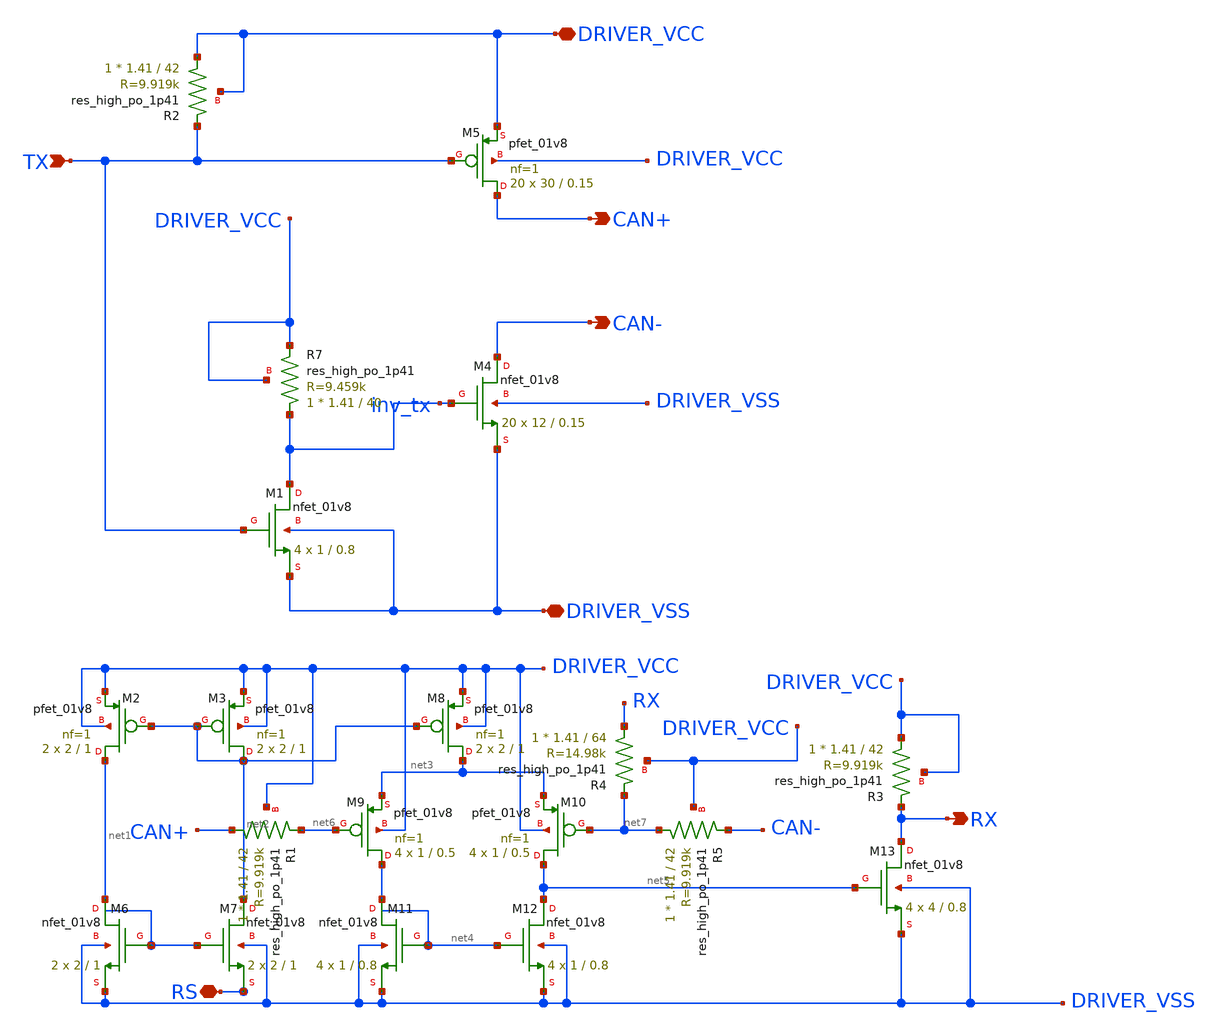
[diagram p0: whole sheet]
** sch_path: ISSCC26/submitted_notebooks/Opensource-ULP-CAN_Transceiver/xschem/can_ic/can_ic.sch
**.subckt can_ic DRIVER_VCC DRIVER_VSS TX CAN+ CAN- RS RX
*.iopin DRIVER_VCC
*.iopin DRIVER_VSS
*.ipin TX
*.opin CAN+
*.opin CAN-
*.iopin RS
*.opin RX
XM4 CAN- inv_tx DRIVER_VSS DRIVER_VSS sky130_fd_pr__nfet_01v8 W=12 L=0.15 ad='int((1 + 1)/2) * 12 / 1 * 0.29'
+ pd='2*int((1 + 1)/2) * (12 / 1 + 0.29)' as='int((1 + 2)/2) * 12 / 1 * 0.29' ps='2*int((1 + 2)/2) * (12 / 1 + 0.29)'
+ nrd='0.29 / 12 ' nrs='0.29 / 12 ' sa=0 sb=0 sd=0 nf=1 mult=20
XM5 CAN+ TX DRIVER_VCC DRIVER_VCC sky130_fd_pr__pfet_01v8 L=0.15 W=30 nf=1 ad='int((1 + 1)/2) * 30 / 1 * 0.29'
+ as='int((1 + 2)/2) * 30 / 1 * 0.29' pd='2*int((1 + 1)/2) * (30 / 1 + 0.29)' ps='2*int((1 + 2)/2) * (30 / 1 + 0.29)'
+ nrd='0.29 / 30 ' nrs='0.29 / 30 ' sa=0 sb=0 sd=0 mult=20 m=20
XM1 inv_tx TX DRIVER_VSS DRIVER_VSS sky130_fd_pr__nfet_01v8 W=1 L=0.8 ad='int((1 + 1)/2) * 1 / 1 * 0.29'
+ pd='2*int((1 + 1)/2) * (1 / 1 + 0.29)' as='int((1 + 2)/2) * 1 / 1 * 0.29' ps='2*int((1 + 2)/2) * (1 / 1 + 0.29)'
+ nrd='0.29 / 1 ' nrs='0.29 / 1 ' sa=0 sb=0 sd=0 nf=1 mult=4
XM2 net1 net2 DRIVER_VCC DRIVER_VCC sky130_fd_pr__pfet_01v8 L=1 W=2 nf=1 ad='int((nf+1)/2) * W/nf * 0.29'
+ as='int((nf+2)/2) * W/nf * 0.29' pd='2*int((nf+1)/2) * (W/nf + 0.29)' ps='2*int((nf+2)/2) * (W/nf + 0.29)'
+ nrd='0.29 / W' nrs='0.29 / W' sa=0 sb=0 sd=0 mult=2 m=2
XM3 net2 net2 DRIVER_VCC DRIVER_VCC sky130_fd_pr__pfet_01v8 L=1 W=2 nf=1 ad='int((nf+1)/2) * W/nf * 0.29'
+ as='int((nf+2)/2) * W/nf * 0.29' pd='2*int((nf+1)/2) * (W/nf + 0.29)' ps='2*int((nf+2)/2) * (W/nf + 0.29)'
+ nrd='0.29 / W' nrs='0.29 / W' sa=0 sb=0 sd=0 mult=2 m=2
XM6 net1 net1 DRIVER_VSS DRIVER_VSS sky130_fd_pr__nfet_01v8 W=2 L=1 ad='int((nf+1)/2) * W/nf * 0.29'
+ pd='2*int((nf+1)/2) * (W/nf + 0.29)' as='int((nf+2)/2) * W/nf * 0.29' ps='2*int((nf+2)/2) * (W/nf + 0.29)'
+ nrd='0.29 / W' nrs='0.29 / W' sa=0 sb=0 sd=0 nf=1 mult=2
XM7 net2 net1 RS DRIVER_VSS sky130_fd_pr__nfet_01v8 W=2 L=1 ad='int((nf+1)/2) * W/nf * 0.29' pd='2*int((nf+1)/2) * (W/nf + 0.29)'
+ as='int((nf+2)/2) * W/nf * 0.29' ps='2*int((nf+2)/2) * (W/nf + 0.29)' nrd='0.29 / W' nrs='0.29 / W' sa=0
+ sb=0 sd=0 nf=1 mult=2
XM8 net3 net2 DRIVER_VCC DRIVER_VCC sky130_fd_pr__pfet_01v8 L=1 W=2 nf=1 ad='int((nf+1)/2) * W/nf * 0.29'
+ as='int((nf+2)/2) * W/nf * 0.29' pd='2*int((nf+1)/2) * (W/nf + 0.29)' ps='2*int((nf+2)/2) * (W/nf + 0.29)'
+ nrd='0.29 / W' nrs='0.29 / W' sa=0 sb=0 sd=0 mult=2 m=2
XM9 net4 net6 net3 DRIVER_VCC sky130_fd_pr__pfet_01v8 L=0.5 W=1 nf=1 ad='int((nf+1)/2) * W/nf * 0.29'
+ as='int((nf+2)/2) * W/nf * 0.29' pd='2*int((nf+1)/2) * (W/nf + 0.29)' ps='2*int((nf+2)/2) * (W/nf + 0.29)'
+ nrd='0.29 / W' nrs='0.29 / W' sa=0 sb=0 sd=0 mult=4 m=4
XM10 net5 net7 net3 DRIVER_VCC sky130_fd_pr__pfet_01v8 L=0.5 W=1 nf=1 ad='int((nf+1)/2) * W/nf * 0.29'
+ as='int((nf+2)/2) * W/nf * 0.29' pd='2*int((nf+1)/2) * (W/nf + 0.29)' ps='2*int((nf+2)/2) * (W/nf + 0.29)'
+ nrd='0.29 / W' nrs='0.29 / W' sa=0 sb=0 sd=0 mult=4 m=4
XM11 net4 net4 DRIVER_VSS DRIVER_VSS sky130_fd_pr__nfet_01v8 W=1 L=0.8 ad='int((nf+1)/2) * W/nf * 0.29'
+ pd='2*int((nf+1)/2) * (W/nf + 0.29)' as='int((nf+2)/2) * W/nf * 0.29' ps='2*int((nf+2)/2) * (W/nf + 0.29)'
+ nrd='0.29 / W' nrs='0.29 / W' sa=0 sb=0 sd=0 nf=1 mult=4
XM12 net5 net4 DRIVER_VSS DRIVER_VSS sky130_fd_pr__nfet_01v8 W=1 L=0.8 ad='int((nf+1)/2) * W/nf * 0.29'
+ pd='2*int((nf+1)/2) * (W/nf + 0.29)' as='int((nf+2)/2) * W/nf * 0.29' ps='2*int((nf+2)/2) * (W/nf + 0.29)'
+ nrd='0.29 / W' nrs='0.29 / W' sa=0 sb=0 sd=0 nf=1 mult=4
XM13 RX net5 DRIVER_VSS DRIVER_VSS sky130_fd_pr__nfet_01v8 W=4 L=0.8 ad='int((nf+1)/2) * W/nf * 0.29'
+ pd='2*int((nf+1)/2) * (W/nf + 0.29)' as='int((nf+2)/2) * W/nf * 0.29' ps='2*int((nf+2)/2) * (W/nf + 0.29)'
+ nrd='0.29 / W' nrs='0.29 / W' sa=0 sb=0 sd=0 nf=1 mult=4
XR7 inv_tx DRIVER_VCC DRIVER_VCC sky130_fd_pr__res_high_po_1p41 L=40 mult=1 m=1
XR5 net7 CAN- DRIVER_VCC sky130_fd_pr__res_high_po_1p41 L=42 mult=1 m=1
XR1 CAN+ net6 DRIVER_VCC sky130_fd_pr__res_high_po_1p41 L=42 mult=1 m=1
XR3 DRIVER_VCC RX DRIVER_VCC sky130_fd_pr__res_high_po_1p41 L=42 mult=1 m=1
XR4 RX net7 DRIVER_VCC sky130_fd_pr__res_high_po_1p41 L=64 mult=1 m=1
XR2 DRIVER_VCC TX DRIVER_VCC sky130_fd_pr__res_high_po_1p41 L=42 mult=1 m=1
**.ends
.end
